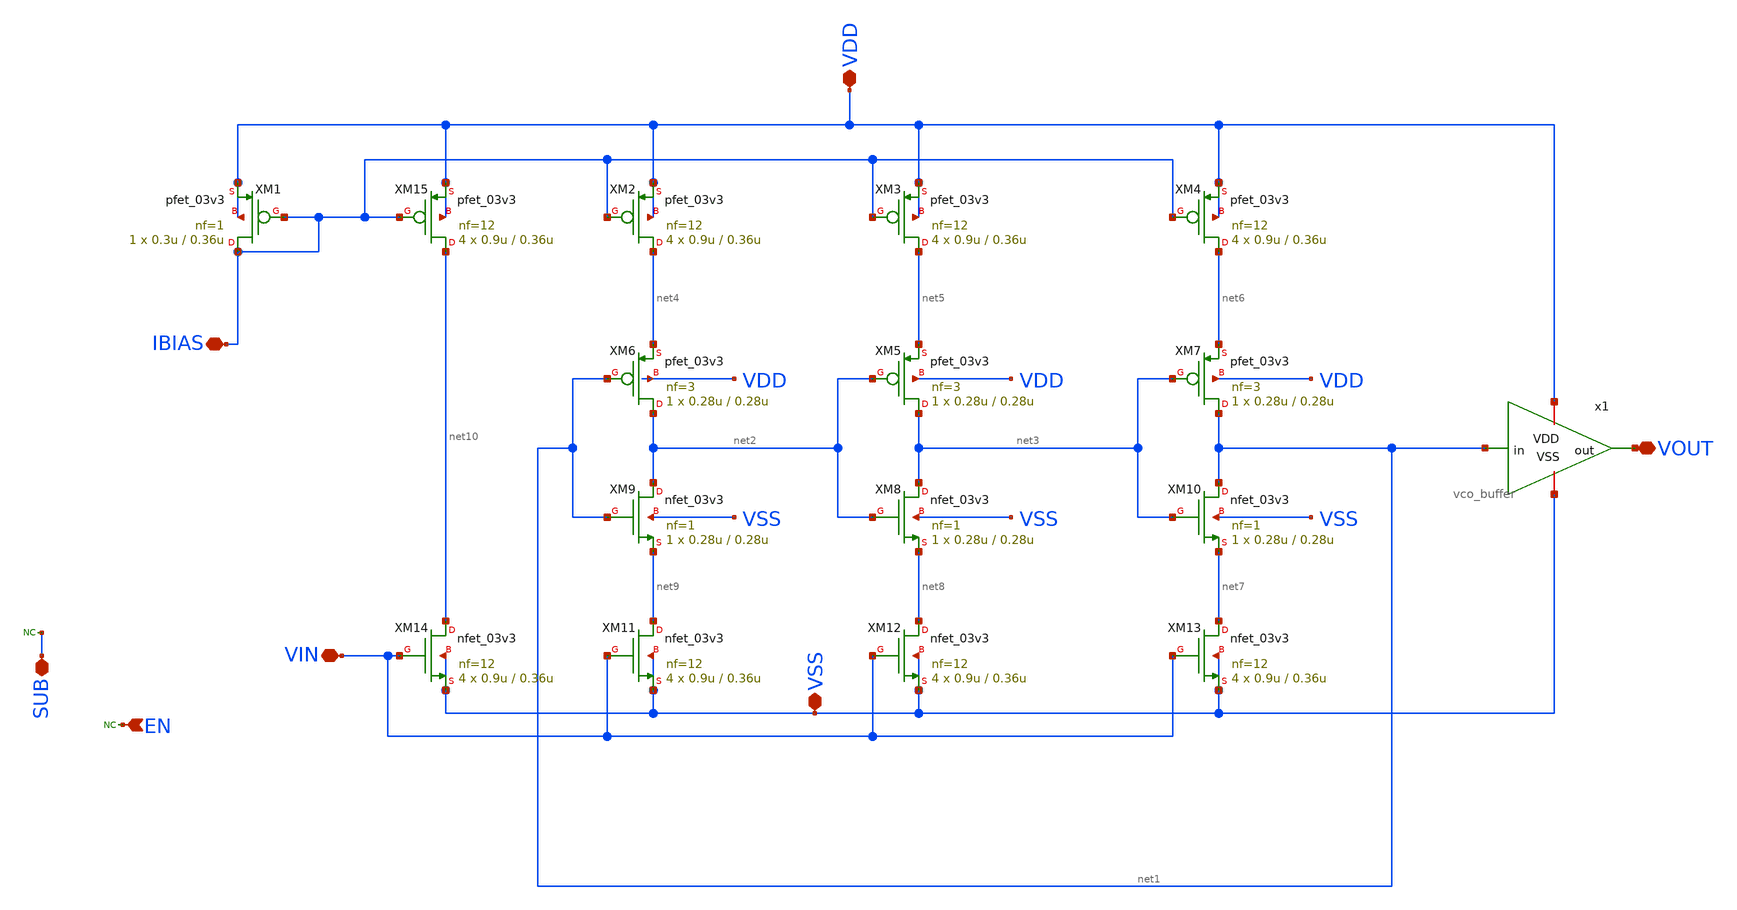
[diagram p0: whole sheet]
** sch_path: designs/untitled.sch
**.subckt untitled VDD VSS SUB IBIAS VOUT EN VIN
*.iopin VDD
*.iopin VSS
*.iopin SUB
*.iopin IBIAS
*.iopin VOUT
*.ipin EN
*.iopin VIN
* noconn SUB
XM1 IBIAS IBIAS VDD VDD pfet_03v3 L=0.36u W=0.3u nf=1 ad='int((nf+1)/2) * W/nf * 0.18u' as='int((nf+2)/2) * W/nf * 0.18u'
+ pd='2*int((nf+1)/2) * (W/nf + 0.18u)' ps='2*int((nf+2)/2) * (W/nf + 0.18u)' nrd='0.18u / W' nrs='0.18u / W'
+ sa=0 sb=0 sd=0 m=1
XM6 net2 net1 net4 VDD pfet_03v3 L=0.28u W=0.28u nf=3 ad='int((nf+1)/2) * W/nf * 0.18u' as='int((nf+2)/2) * W/nf * 0.18u'
+ pd='2*int((nf+1)/2) * (W/nf + 0.18u)' ps='2*int((nf+2)/2) * (W/nf + 0.18u)' nrd='0.18u / W' nrs='0.18u / W'
+ sa=0 sb=0 sd=0 m=1
XM14 net10 VIN VSS VSS nfet_03v3 L=0.36u W=0.9u nf=12 ad='int((nf+1)/2) * W/nf * 0.18u' as='int((nf+2)/2) * W/nf * 0.18u'
+ pd='2*int((nf+1)/2) * (W/nf + 0.18u)' ps='2*int((nf+2)/2) * (W/nf + 0.18u)' nrd='0.18u / W' nrs='0.18u / W'
+ sa=0 sb=0 sd=0 m=4
XM15 net10 IBIAS VDD VDD pfet_03v3 L=0.36u W=0.9u nf=12 ad='int((nf+1)/2) * W/nf * 0.18u' as='int((nf+2)/2) * W/nf * 0.18u'
+ pd='2*int((nf+1)/2) * (W/nf + 0.18u)' ps='2*int((nf+2)/2) * (W/nf + 0.18u)' nrd='0.18u / W' nrs='0.18u / W'
+ sa=0 sb=0 sd=0 m=4
x1 VDD net1 VOUT VSS vco_buffer
XM9 net2 net1 net9 VSS nfet_03v3 L=0.28u W=0.28u nf=1 ad='int((nf+1)/2) * W/nf * 0.18u' as='int((nf+2)/2) * W/nf * 0.18u'
+ pd='2*int((nf+1)/2) * (W/nf + 0.18u)' ps='2*int((nf+2)/2) * (W/nf + 0.18u)' nrd='0.18u / W' nrs='0.18u / W'
+ sa=0 sb=0 sd=0 m=1
XM8 net3 net2 net8 VSS nfet_03v3 L=0.28u W=0.28u nf=1 ad='int((nf+1)/2) * W/nf * 0.18u' as='int((nf+2)/2) * W/nf * 0.18u'
+ pd='2*int((nf+1)/2) * (W/nf + 0.18u)' ps='2*int((nf+2)/2) * (W/nf + 0.18u)' nrd='0.18u / W' nrs='0.18u / W'
+ sa=0 sb=0 sd=0 m=1
XM10 net1 net3 net7 VSS nfet_03v3 L=0.28u W=0.28u nf=1 ad='int((nf+1)/2) * W/nf * 0.18u' as='int((nf+2)/2) * W/nf * 0.18u'
+ pd='2*int((nf+1)/2) * (W/nf + 0.18u)' ps='2*int((nf+2)/2) * (W/nf + 0.18u)' nrd='0.18u / W' nrs='0.18u / W'
+ sa=0 sb=0 sd=0 m=1
XM2 net4 IBIAS VDD VDD pfet_03v3 L=0.36u W=0.9u nf=12 ad='int((nf+1)/2) * W/nf * 0.18u' as='int((nf+2)/2) * W/nf * 0.18u'
+ pd='2*int((nf+1)/2) * (W/nf + 0.18u)' ps='2*int((nf+2)/2) * (W/nf + 0.18u)' nrd='0.18u / W' nrs='0.18u / W'
+ sa=0 sb=0 sd=0 m=4
XM3 net5 IBIAS VDD VDD pfet_03v3 L=0.36u W=0.9u nf=12 ad='int((nf+1)/2) * W/nf * 0.18u' as='int((nf+2)/2) * W/nf * 0.18u'
+ pd='2*int((nf+1)/2) * (W/nf + 0.18u)' ps='2*int((nf+2)/2) * (W/nf + 0.18u)' nrd='0.18u / W' nrs='0.18u / W'
+ sa=0 sb=0 sd=0 m=4
XM4 net6 IBIAS VDD VDD pfet_03v3 L=0.36u W=0.9u nf=12 ad='int((nf+1)/2) * W/nf * 0.18u' as='int((nf+2)/2) * W/nf * 0.18u'
+ pd='2*int((nf+1)/2) * (W/nf + 0.18u)' ps='2*int((nf+2)/2) * (W/nf + 0.18u)' nrd='0.18u / W' nrs='0.18u / W'
+ sa=0 sb=0 sd=0 m=4
XM11 net9 VIN VSS VSS nfet_03v3 L=0.36u W=0.9u nf=12 ad='int((nf+1)/2) * W/nf * 0.18u' as='int((nf+2)/2) * W/nf * 0.18u'
+ pd='2*int((nf+1)/2) * (W/nf + 0.18u)' ps='2*int((nf+2)/2) * (W/nf + 0.18u)' nrd='0.18u / W' nrs='0.18u / W'
+ sa=0 sb=0 sd=0 m=4
XM12 net8 VIN VSS VSS nfet_03v3 L=0.36u W=0.9u nf=12 ad='int((nf+1)/2) * W/nf * 0.18u' as='int((nf+2)/2) * W/nf * 0.18u'
+ pd='2*int((nf+1)/2) * (W/nf + 0.18u)' ps='2*int((nf+2)/2) * (W/nf + 0.18u)' nrd='0.18u / W' nrs='0.18u / W'
+ sa=0 sb=0 sd=0 m=4
XM13 net7 VIN VSS VSS nfet_03v3 L=0.36u W=0.9u nf=12 ad='int((nf+1)/2) * W/nf * 0.18u' as='int((nf+2)/2) * W/nf * 0.18u'
+ pd='2*int((nf+1)/2) * (W/nf + 0.18u)' ps='2*int((nf+2)/2) * (W/nf + 0.18u)' nrd='0.18u / W' nrs='0.18u / W'
+ sa=0 sb=0 sd=0 m=4
XM5 net3 net2 net5 VDD pfet_03v3 L=0.28u W=0.28u nf=3 ad='int((nf+1)/2) * W/nf * 0.18u' as='int((nf+2)/2) * W/nf * 0.18u'
+ pd='2*int((nf+1)/2) * (W/nf + 0.18u)' ps='2*int((nf+2)/2) * (W/nf + 0.18u)' nrd='0.18u / W' nrs='0.18u / W'
+ sa=0 sb=0 sd=0 m=1
XM7 net1 net3 net6 VDD pfet_03v3 L=0.28u W=0.28u nf=3 ad='int((nf+1)/2) * W/nf * 0.18u' as='int((nf+2)/2) * W/nf * 0.18u'
+ pd='2*int((nf+1)/2) * (W/nf + 0.18u)' ps='2*int((nf+2)/2) * (W/nf + 0.18u)' nrd='0.18u / W' nrs='0.18u / W'
+ sa=0 sb=0 sd=0 m=1
* noconn EN
**.ends

* expanding   symbol:  libs/core_vco/vco_buffer/vco_buffer.sym # of pins=4
** sym_path: designs/libs/core_vco/vco_buffer/vco_buffer.sym
** sch_path: designs/libs/core_vco/vco_buffer/vco_buffer.sch
.subckt vco_buffer VDD in out VSS
*.ipin in
*.opin out
*.iopin VDD
*.iopin VSS
XM16 net1 in VDD VDD pfet_03v3 L=0.28u W=2u nf=2 ad='int((nf+1)/2) * W/nf * 0.18u' as='int((nf+2)/2) * W/nf * 0.18u'
+ pd='2*int((nf+1)/2) * (W/nf + 0.18u)' ps='2*int((nf+2)/2) * (W/nf + 0.18u)' nrd='0.18u / W' nrs='0.18u / W'
+ sa=0 sb=0 sd=0 m=1
XM17 net1 in VSS VSS nfet_03v3 L=0.28u W=1u nf=1 ad='int((nf+1)/2) * W/nf * 0.18u' as='int((nf+2)/2) * W/nf * 0.18u'
+ pd='2*int((nf+1)/2) * (W/nf + 0.18u)' ps='2*int((nf+2)/2) * (W/nf + 0.18u)' nrd='0.18u / W' nrs='0.18u / W'
+ sa=0 sb=0 sd=0 m=1
XM2 out net1 VSS VSS nfet_03v3 L=0.28u W=1u nf=1 ad='int((nf+1)/2) * W/nf * 0.18u' as='int((nf+2)/2) * W/nf * 0.18u'
+ pd='2*int((nf+1)/2) * (W/nf + 0.18u)' ps='2*int((nf+2)/2) * (W/nf + 0.18u)' nrd='0.18u / W' nrs='0.18u / W'
+ sa=0 sb=0 sd=0 m=1
XM1 out net1 VDD VDD pfet_03v3 L=0.28u W=2u nf=2 ad='int((nf+1)/2) * W/nf * 0.18u' as='int((nf+2)/2) * W/nf * 0.18u'
+ pd='2*int((nf+1)/2) * (W/nf + 0.18u)' ps='2*int((nf+2)/2) * (W/nf + 0.18u)' nrd='0.18u / W' nrs='0.18u / W'
+ sa=0 sb=0 sd=0 m=1
.ends

.end
